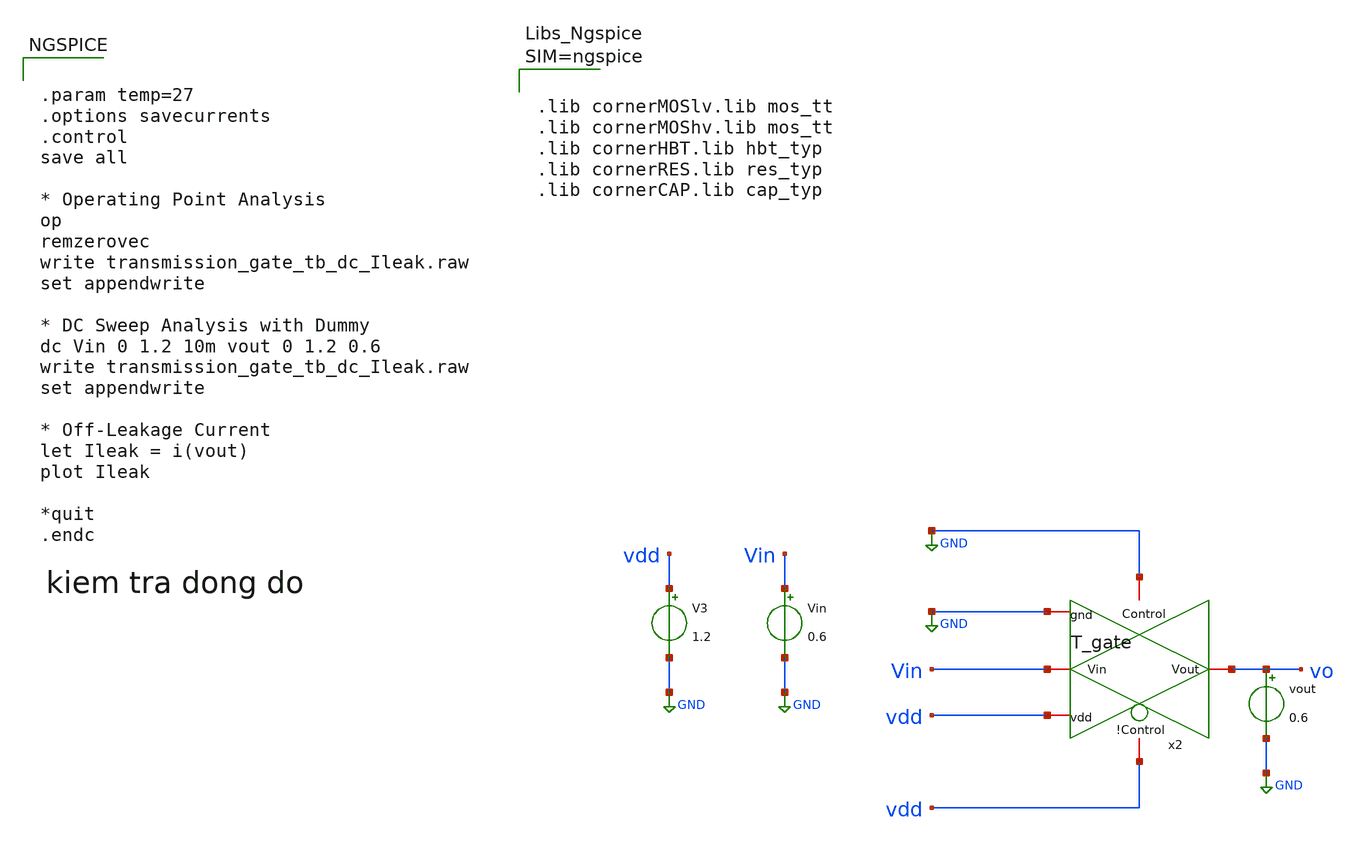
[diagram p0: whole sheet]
** sch_path: xschem/T_gate_tb_dc_ileak.sch
**.subckt T_gate_tb_dc_ileak
x2 vdd Vin vo GND GND vdd T_gate
Vin Vin GND 0.6
V3 vdd GND 1.2
vout vo GND 0.6
**** begin user architecture code


.param temp=27
.options savecurrents
.control
save all

* Operating Point Analysis
op
remzerovec
write transmission_gate_tb_dc_Ileak.raw
set appendwrite

* DC Sweep Analysis with Dummy
dc Vin 0 1.2 10m vout 0 1.2 0.6
write transmission_gate_tb_dc_Ileak.raw
set appendwrite

* Off-Leakage Current
let Ileak = i(vout)
plot Ileak

*quit
.endc




.lib cornerMOSlv.lib mos_tt
.lib cornerMOShv.lib mos_tt
.lib cornerHBT.lib hbt_typ
.lib cornerRES.lib res_typ
.lib cornerCAP.lib cap_typ



**** end user architecture code
**.ends

* expanding   symbol:
*+  /home/designer/shared/IHP-AnalogAcademy/modules/module_3_8_bit_SAR_ADC/part_2_digital_comps/T_gate/schematic/T_gate.sym # of pins=6
** sym_path: /home/designer/shared/IHP-AnalogAcademy/modules/module_3_8_bit_SAR_ADC/part_2_digital_comps/T_gate/schematic/T_gate.sym
** sch_path: /home/designer/shared/IHP-AnalogAcademy/modules/module_3_8_bit_SAR_ADC/part_2_digital_comps/T_gate/schematic/T_gate.sch
.subckt T_gate !Control Vin Vout gnd Control vdd
*.iopin Vout
*.iopin Vin
*.iopin !Control
*.iopin Control
*.iopin gnd
*.iopin vdd
XM1 Vin Control Vout gnd sg13_lv_nmos w=1u l=0.13u ng=1 m=1 mm_ok=1
XM2 Vout !Control Vin vdd sg13_lv_pmos w=3u l=0.13u ng=1 m=1 mm_ok=1
.ends

.GLOBAL GND
.end
